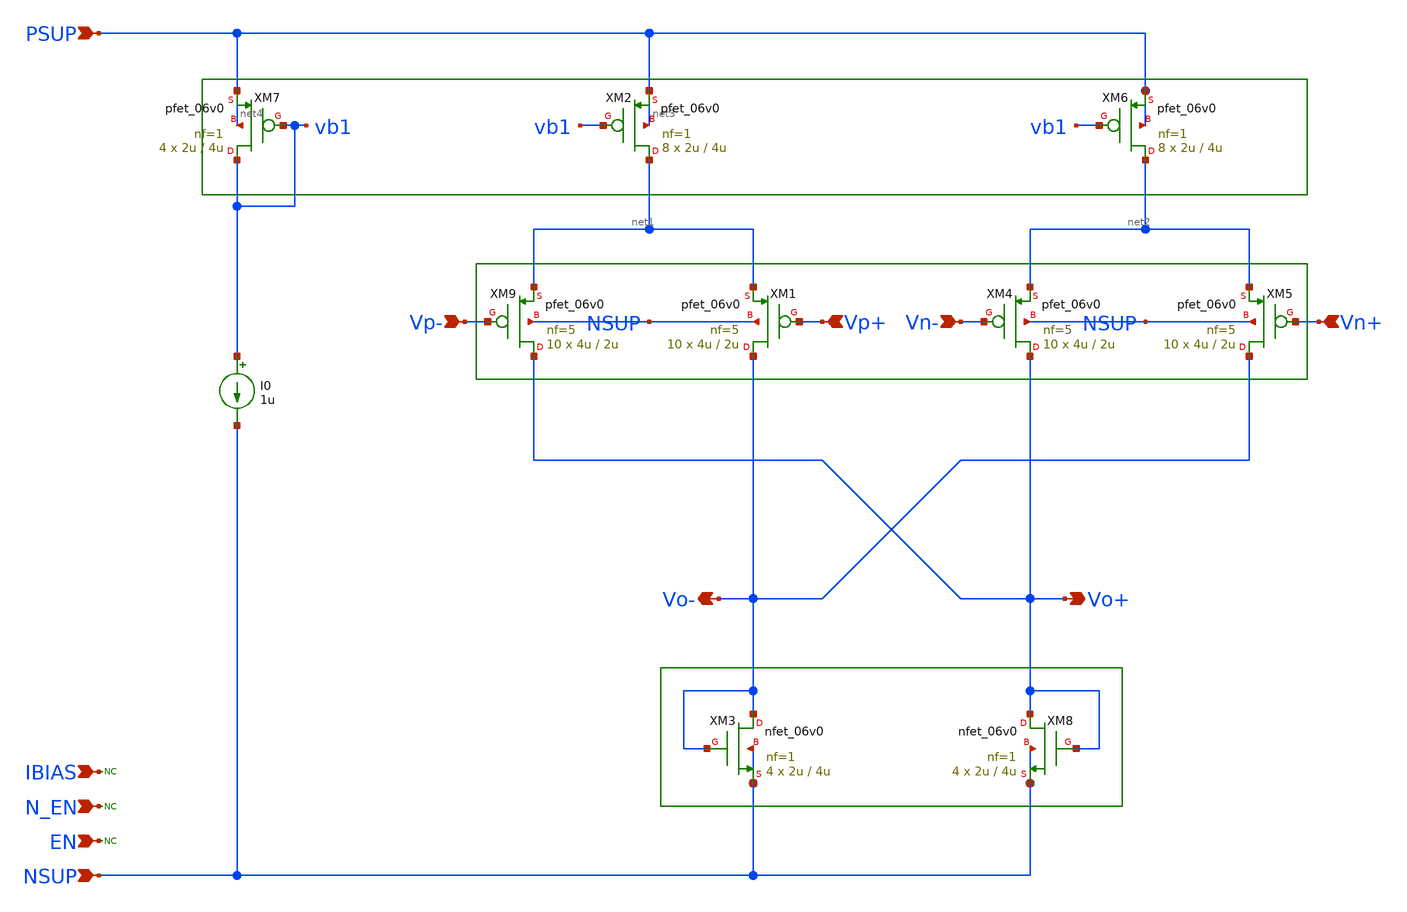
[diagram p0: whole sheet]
** sch_path: xschem/blocks/fdda/fdda.sch
**.subckt fdda PSUP NSUP N_EN EN IBIAS Vp+ Vp- Vn+ Vn- Vo+ Vo-
*.ipin PSUP
*.ipin NSUP
*.ipin N_EN
*.ipin EN
*.ipin IBIAS
*.ipin Vp+
*.ipin Vp-
*.ipin Vn+
*.ipin Vn-
*.opin Vo+
*.opin Vo-
* noconn N_EN
* noconn EN
I0 vb1 NSUP 1u
XM9 Vo+ Vp- net1 NSUP pfet_06v0 L=2u W=4u nf=5 ad='int((nf+1)/2) * W/nf * 0.18u' as='int((nf+2)/2) * W/nf * 0.18u'
+ pd='2*int((nf+1)/2) * (W/nf + 0.18u)' ps='2*int((nf+2)/2) * (W/nf + 0.18u)' nrd='0.18u / W' nrs='0.18u / W'
+ sa=0 sb=0 sd=0 m=10
XM1 Vo- Vp+ net1 NSUP pfet_06v0 L=2u W=4u nf=5 ad='int((nf+1)/2) * W/nf * 0.18u' as='int((nf+2)/2) * W/nf * 0.18u'
+ pd='2*int((nf+1)/2) * (W/nf + 0.18u)' ps='2*int((nf+2)/2) * (W/nf + 0.18u)' nrd='0.18u / W' nrs='0.18u / W'
+ sa=0 sb=0 sd=0 m=10
XM2 net1 vb1 PSUP net3 pfet_06v0 L=4u W=2u nf=1 ad='int((nf+1)/2) * W/nf * 0.18u' as='int((nf+2)/2) * W/nf * 0.18u'
+ pd='2*int((nf+1)/2) * (W/nf + 0.18u)' ps='2*int((nf+2)/2) * (W/nf + 0.18u)' nrd='0.18u / W' nrs='0.18u / W'
+ sa=0 sb=0 sd=0 m=8
XM3 Vo- Vo- NSUP NSUP nfet_06v0 L=4u W=2u nf=1 ad='int((nf+1)/2) * W/nf * 0.18u' as='int((nf+2)/2) * W/nf * 0.18u'
+ pd='2*int((nf+1)/2) * (W/nf + 0.18u)' ps='2*int((nf+2)/2) * (W/nf + 0.18u)' nrd='0.18u / W' nrs='0.18u / W'
+ sa=0 sb=0 sd=0 m=4
XM4 Vo+ Vn- net2 NSUP pfet_06v0 L=2u W=4u nf=5 ad='int((nf+1)/2) * W/nf * 0.18u' as='int((nf+2)/2) * W/nf * 0.18u'
+ pd='2*int((nf+1)/2) * (W/nf + 0.18u)' ps='2*int((nf+2)/2) * (W/nf + 0.18u)' nrd='0.18u / W' nrs='0.18u / W'
+ sa=0 sb=0 sd=0 m=10
XM5 Vo- Vn+ net2 NSUP pfet_06v0 L=2u W=4u nf=5 ad='int((nf+1)/2) * W/nf * 0.18u' as='int((nf+2)/2) * W/nf * 0.18u'
+ pd='2*int((nf+1)/2) * (W/nf + 0.18u)' ps='2*int((nf+2)/2) * (W/nf + 0.18u)' nrd='0.18u / W' nrs='0.18u / W'
+ sa=0 sb=0 sd=0 m=10
XM6 net2 vb1 PSUP PSUP pfet_06v0 L=4u W=2u nf=1 ad='int((nf+1)/2) * W/nf * 0.18u' as='int((nf+2)/2) * W/nf * 0.18u'
+ pd='2*int((nf+1)/2) * (W/nf + 0.18u)' ps='2*int((nf+2)/2) * (W/nf + 0.18u)' nrd='0.18u / W' nrs='0.18u / W'
+ sa=0 sb=0 sd=0 m=8
XM8 Vo+ Vo+ NSUP NSUP nfet_06v0 L=4u W=2u nf=1 ad='int((nf+1)/2) * W/nf * 0.18u' as='int((nf+2)/2) * W/nf * 0.18u'
+ pd='2*int((nf+1)/2) * (W/nf + 0.18u)' ps='2*int((nf+2)/2) * (W/nf + 0.18u)' nrd='0.18u / W' nrs='0.18u / W'
+ sa=0 sb=0 sd=0 m=4
XM7 vb1 vb1 PSUP net4 pfet_06v0 L=4u W=2u nf=1 ad='int((nf+1)/2) * W/nf * 0.18u' as='int((nf+2)/2) * W/nf * 0.18u'
+ pd='2*int((nf+1)/2) * (W/nf + 0.18u)' ps='2*int((nf+2)/2) * (W/nf + 0.18u)' nrd='0.18u / W' nrs='0.18u / W'
+ sa=0 sb=0 sd=0 m=4
* noconn IBIAS
**.ends
.end
